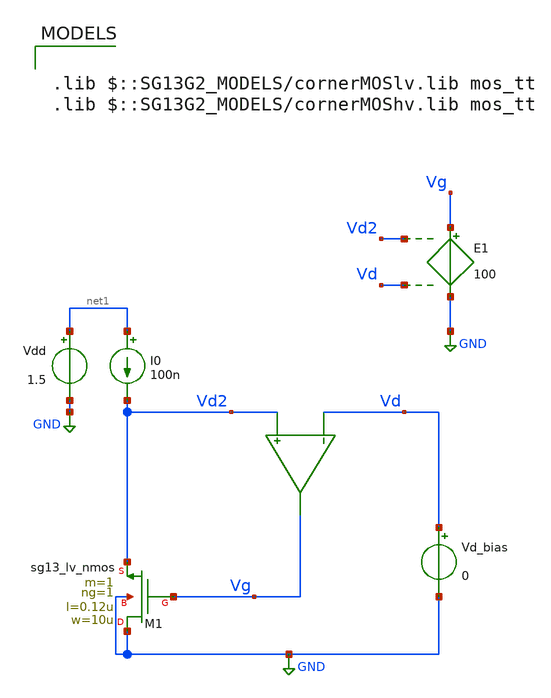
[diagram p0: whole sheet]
** sch_path: legacy/Examples/IHP-SG13/xschem/Extraction/nmos_sigma_ext.sch
**.subckt nmos_sigma_ext
I0 net1 Vd2 100n
Vd_bias Vd GND 0
Vdd net1 GND 1.5
XM1 GND Vg Vd2 GND sg13_lv_nmos w=10u l=0.12u ng=1 m=1 mm_ok=1
E1 Vg GND Vd2 Vd 100
**** begin user architecture code



.option gmin = 1e-18

.nodeset V(vd2)=1.5

.control
pre_osdi ./psp103_nqs.osdi
save all

dc Vd_bias 0.05 1.5 25.9m

let vd_interp = 1.5/3
let sigma = -deriv(V(vg))/deriv(V(vd))
save sigma

echo
echo
echo


echo Sigma @ VD=$&vd_interp:
meas dc sigma_value FIND sigma WHEN V(vd)=vd_interp

echo
echo
echo
write nmos_sigma_ext.raw

.endc





.lib $::SG13G2_MODELS/cornerMOSlv.lib mos_tt
.lib $::SG13G2_MODELS/cornerMOShv.lib mos_tt

**** end user architecture code
**.ends
.GLOBAL GND
.end
